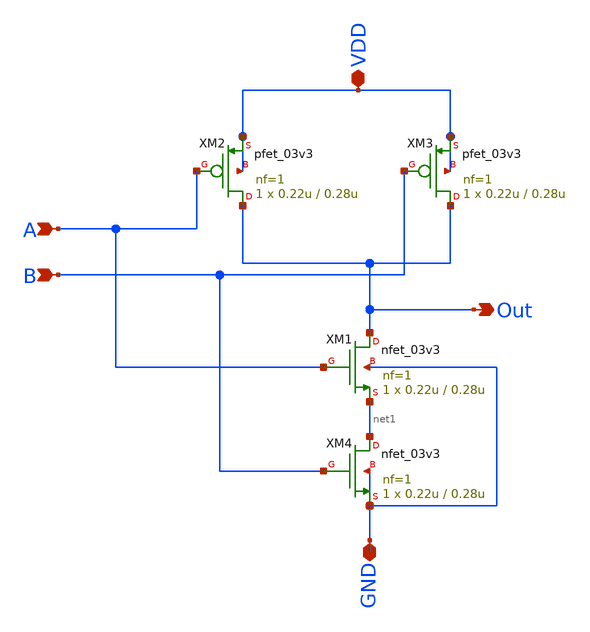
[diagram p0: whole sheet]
** sch_path: 2bit_Comparator/2x_drive/my_nand.sch
**.subckt my_nand A Out B VDD GND
*.ipin A
*.opin Out
*.ipin B
*.iopin VDD
*.iopin GND
XM1 Out A net1 GND nfet_03v3 L=0.28u W=0.22u nf=1 ad='int((nf+1)/2) * W/nf * 0.18u' as='int((nf+2)/2) * W/nf * 0.18u'
+ pd='2*int((nf+1)/2) * (W/nf + 0.18u)' ps='2*int((nf+2)/2) * (W/nf + 0.18u)' nrd='0.18u / W' nrs='0.18u / W'
+ sa=0 sb=0 sd=0 m=1
XM2 Out A VDD VDD pfet_03v3 L=0.28u W=0.22u nf=1 ad='int((nf+1)/2) * W/nf * 0.18u' as='int((nf+2)/2) * W/nf * 0.18u'
+ pd='2*int((nf+1)/2) * (W/nf + 0.18u)' ps='2*int((nf+2)/2) * (W/nf + 0.18u)' nrd='0.18u / W' nrs='0.18u / W'
+ sa=0 sb=0 sd=0 m=1
XM3 Out B VDD VDD pfet_03v3 L=0.28u W=0.22u nf=1 ad='int((nf+1)/2) * W/nf * 0.18u' as='int((nf+2)/2) * W/nf * 0.18u'
+ pd='2*int((nf+1)/2) * (W/nf + 0.18u)' ps='2*int((nf+2)/2) * (W/nf + 0.18u)' nrd='0.18u / W' nrs='0.18u / W'
+ sa=0 sb=0 sd=0 m=1
XM4 net1 B GND GND nfet_03v3 L=0.28u W=0.22u nf=1 ad='int((nf+1)/2) * W/nf * 0.18u' as='int((nf+2)/2) * W/nf * 0.18u'
+ pd='2*int((nf+1)/2) * (W/nf + 0.18u)' ps='2*int((nf+2)/2) * (W/nf + 0.18u)' nrd='0.18u / W' nrs='0.18u / W'
+ sa=0 sb=0 sd=0 m=1
**.ends
.end
